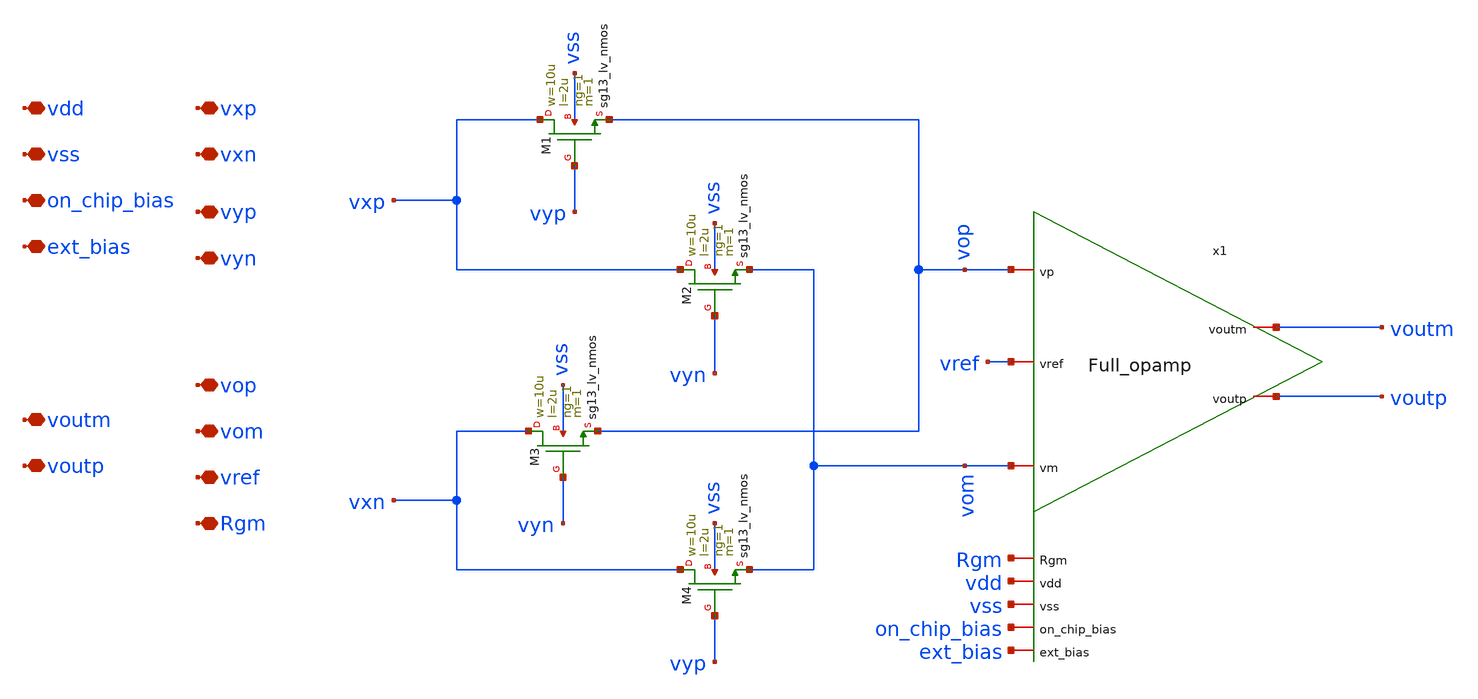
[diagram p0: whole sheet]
** sch_path: src/Multiplier/Src/multiplier.sch
**.subckt multiplier vxp vxn vyp vyn vop vom vref Rgm vdd vss on_chip_bias ext_bias voutm voutp
*.iopin vxp
*.iopin vxn
*.iopin vyp
*.iopin vyn
*.iopin vop
*.iopin vom
*.iopin vref
*.iopin Rgm
*.iopin vdd
*.iopin vss
*.iopin on_chip_bias
*.iopin ext_bias
*.iopin voutm
*.iopin voutp
x1 on_chip_bias vref vdd voutm ext_bias vom voutp vss vop Rgm Full_opamp
XM1 vxp vyp vop vss sg13_lv_nmos w=10u l=2u ng=1 m=1 mm_ok=1
XM2 vxp vyn vom vss sg13_lv_nmos w=10u l=2u ng=1 m=1 mm_ok=1
XM3 vxn vyn vop vss sg13_lv_nmos w=10u l=2u ng=1 m=1 mm_ok=1
XM4 vxn vyp vom vss sg13_lv_nmos w=10u l=2u ng=1 m=1 mm_ok=1
**.ends
.end
